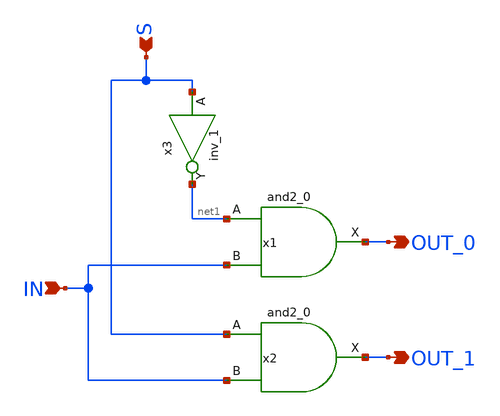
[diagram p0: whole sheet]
** sch_path: demux2.sch
**.subckt demux2 S OUT_0 IN OUT_1
*.ipin S
*.opin OUT_0
*.ipin IN
*.opin OUT_1
x1 net1 IN VGND VNB VPB VPWR OUT_0 sky130_fd_sc_hd__and2_0
x2 S IN VGND VNB VPB VPWR OUT_1 sky130_fd_sc_hd__and2_0
x3 S VGND VNB VPB VPWR net1 sky130_fd_sc_hd__inv_1
**.ends
.end
